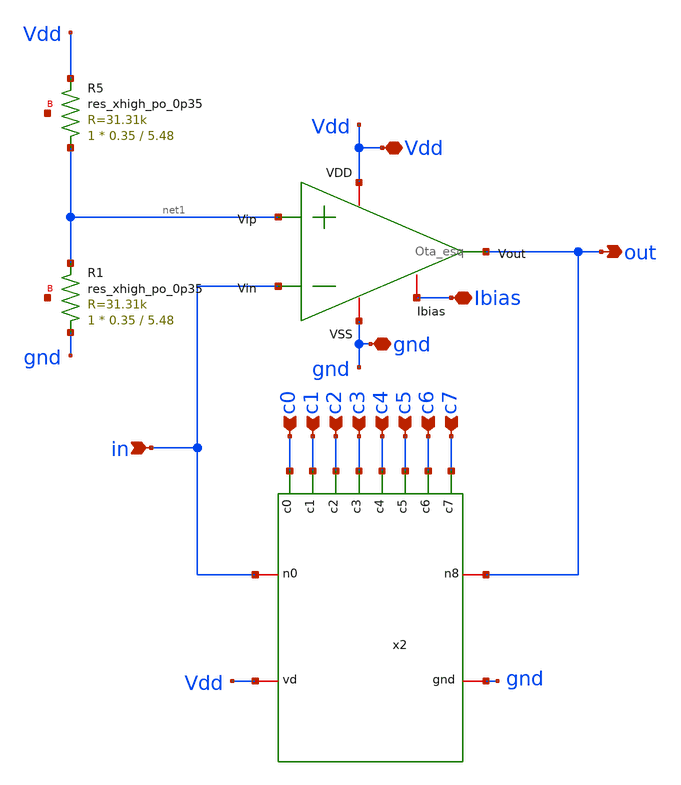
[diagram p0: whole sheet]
** sch_path: xschem/dpga.sch
**.subckt dpga in Vdd gnd Ibias out c0 c1 c2 c3 c4 c5 c6 c7
*.ipin in
*.iopin Vdd
*.iopin gnd
*.iopin Ibias
*.opin out
*.ipin c0
*.ipin c1
*.ipin c2
*.ipin c3
*.ipin c4
*.ipin c5
*.ipin c6
*.ipin c7
x1 Vdd in net1 out Ibias gnd Ota_esq
x2 gnd Vdd c5 c1 c2 c6 c7 c3 c0 c4 out in digpot
XR5 net1 Vdd net2 sky130_fd_pr__res_xhigh_po_0p35 L=5.48 mult=1 m=1
XR1 gnd net1 net3 sky130_fd_pr__res_xhigh_po_0p35 L=5.48 mult=1 m=1
**.ends

* expanding   symbol:  Ota_esq.sym # of pins=6
** sym_path: Ota_esq.sym
** sch_path: Ota_esq.sch
.subckt Ota_esq VDD Vin Vip Vout Ibias VSS
*.ipin Vin
*.ipin Vip
*.iopin VDD
*.iopin VSS
*.iopin Ibias
*.opin Vout
XM1 net1 Vin net3 net3 sky130_fd_pr__pfet_01v8 L=1 W=1 nf=1 ad='int((nf+1)/2) * W/nf * 0.29' as='int((nf+2)/2) * W/nf * 0.29'
+ pd='2*int((nf+1)/2) * (W/nf + 0.29)' ps='2*int((nf+2)/2) * (W/nf + 0.29)' nrd='0.29 / W' nrs='0.29 / W'
+ sa=0 sb=0 sd=0 mult=1 m=1
XM2 net2 Vip net3 net3 sky130_fd_pr__pfet_01v8 L=1 W=1 nf=1 ad='int((nf+1)/2) * W/nf * 0.29' as='int((nf+2)/2) * W/nf * 0.29'
+ pd='2*int((nf+1)/2) * (W/nf + 0.29)' ps='2*int((nf+2)/2) * (W/nf + 0.29)' nrd='0.29 / W' nrs='0.29 / W'
+ sa=0 sb=0 sd=0 mult=1 m=1
XM3 net1 net1 VSS VSS sky130_fd_pr__nfet_01v8 L=8 W=0.5 nf=1 ad='int((nf+1)/2) * W/nf * 0.29' as='int((nf+2)/2) * W/nf * 0.29'
+ pd='2*int((nf+1)/2) * (W/nf + 0.29)' ps='2*int((nf+2)/2) * (W/nf + 0.29)' nrd='0.29 / W' nrs='0.29 / W'
+ sa=0 sb=0 sd=0 mult=1 m=1
XM4 net2 net1 VSS VSS sky130_fd_pr__nfet_01v8 L=8 W=0.5 nf=1 ad='int((nf+1)/2) * W/nf * 0.29' as='int((nf+2)/2) * W/nf * 0.29'
+ pd='2*int((nf+1)/2) * (W/nf + 0.29)' ps='2*int((nf+2)/2) * (W/nf + 0.29)' nrd='0.29 / W' nrs='0.29 / W'
+ sa=0 sb=0 sd=0 mult=1 m=1
XM5 net3 Ibias VDD VDD sky130_fd_pr__pfet_01v8 L=1 W=23.256 nf=1 ad='int((nf+1)/2) * W/nf * 0.29' as='int((nf+2)/2) * W/nf * 0.29'
+ pd='2*int((nf+1)/2) * (W/nf + 0.29)' ps='2*int((nf+2)/2) * (W/nf + 0.29)' nrd='0.29 / W' nrs='0.29 / W'
+ sa=0 sb=0 sd=0 mult=1 m=1
XM8 Ibias Ibias VDD VDD sky130_fd_pr__pfet_01v8 L=1 W=23.256 nf=1 ad='int((nf+1)/2) * W/nf * 0.29' as='int((nf+2)/2) * W/nf * 0.29'
+ pd='2*int((nf+1)/2) * (W/nf + 0.29)' ps='2*int((nf+2)/2) * (W/nf + 0.29)' nrd='0.29 / W' nrs='0.29 / W'
+ sa=0 sb=0 sd=0 mult=1 m=1
XM6 Vout Ibias VDD VDD sky130_fd_pr__pfet_01v8 L=1 W=40.183 nf=1 ad='int((nf+1)/2) * W/nf * 0.29' as='int((nf+2)/2) * W/nf * 0.29'
+ pd='2*int((nf+1)/2) * (W/nf + 0.29)' ps='2*int((nf+2)/2) * (W/nf + 0.29)' nrd='0.29 / W' nrs='0.29 / W'
+ sa=0 sb=0 sd=0 mult=1 m=1
XM7 Vout net2 VSS VSS sky130_fd_pr__nfet_01v8 L=1 W=21.509 nf=1 ad='int((nf+1)/2) * W/nf * 0.29' as='int((nf+2)/2) * W/nf * 0.29'
+ pd='2*int((nf+1)/2) * (W/nf + 0.29)' ps='2*int((nf+2)/2) * (W/nf + 0.29)' nrd='0.29 / W' nrs='0.29 / W'
+ sa=0 sb=0 sd=0 mult=1 m=1
XC1 net2 Vout sky130_fd_pr__cap_mim_m3_1 W=23 L=23 MF=1 m=1
.ends


* expanding   symbol:  digpot.sym # of pins=12
** sym_path: xschem/digpot.sym
** sch_path: xschem/digpot.sch
.subckt digpot gnd vd c5 c1 c2 c6 c7 c3 c0 c4 n8 n0
*.ipin c0
*.ipin c1
*.ipin c2
*.ipin c3
*.ipin c4
*.ipin c5
*.ipin c6
*.ipin c7
*.iopin gnd
*.iopin vd
*.iopin n0
*.iopin n8
XR0 n1 n0 gnd sky130_fd_pr__res_high_po_0p35 L=0.98 mult=1 m=1
XR1 n2 n1 gnd sky130_fd_pr__res_high_po_0p35 L=2.07 mult=1 m=1
XR2 n3 n2 gnd sky130_fd_pr__res_xhigh_po_0p35 L=0.58 mult=1 m=1
XR3 n4 n3 gnd sky130_fd_pr__res_xhigh_po_0p35 L=1.28 mult=1 m=1
XR4 n5 n4 gnd sky130_fd_pr__res_xhigh_po_0p35 L=2.68 mult=1 m=1
XR5 n6 n5 gnd sky130_fd_pr__res_xhigh_po_0p35 L=5.48 mult=1 m=1
XR6 n7 n6 gnd sky130_fd_pr__res_xhigh_po_0p35 L=10.73 mult=1 m=1
XR7 n8 n7 gnd sky130_fd_pr__res_xhigh_po_0p35 L=22.28 mult=1 m=1
G1 n1 n0 vcr pwl(1) c0 gnd 1.0 1G 2.0 10
G2 n2 n1 vcr pwl(1) c1 gnd 1.0 1G 2.0 10
G3 n3 n2 vcr pwl(1) c2 gnd 1.0 1G 2.0 10
G4 n4 n3 vcr pwl(1) c3 gnd 1.0 1G 2.0 10
G5 n5 n4 vcr pwl(1) c4 gnd 1.0 1G 2.0 10
G6 n6 n5 vcr pwl(1) c5 gnd 1.0 1G 2.0 10
G7 n7 n6 vcr pwl(1) c6 gnd 1.0 1G 2.0 10
G8 n8 n7 vcr pwl(1) c7 gnd 1.0 1G 2.0 10
.ends

.end
